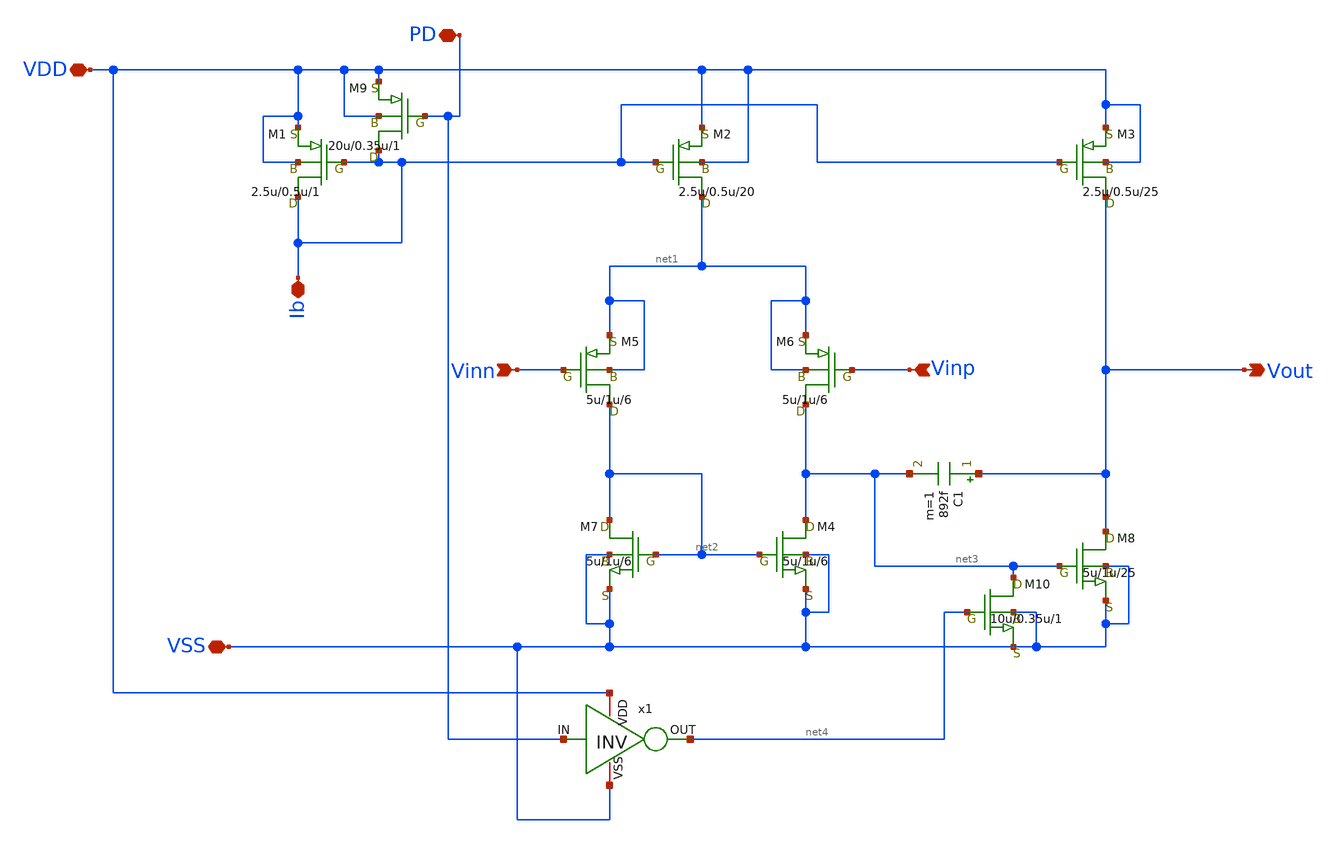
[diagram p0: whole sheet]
** sch_path: OPAmpP.sch
**.subckt OPAmpP Vout Vinn Vinp Ib VDD VSS PD
*.opin Vout
*.ipin Vinn
*.ipin Vinp
*.iopin Ib
*.iopin VDD
*.iopin VSS
*.iopin PD
M1 Ib Ib VDD VDD pch w=2.5u l=0.5u as=0 ps=0 ad=0 pd=0 m=1
M2 net1 Ib VDD VDD pch w=2.5u l=0.5u as=0 ps=0 ad=0 pd=0 m=20
M3 Vout Ib VDD VDD pch w=2.5u l=0.5u as=0 ps=0 ad=0 pd=0 m=25
M4 net3 net2 VSS VSS nch w=5u l=1u as=0 ps=0 ad=0 pd=0 m=6
M5 net2 Vinn net1 net1 pch w=5u l=1u as=0 ps=0 ad=0 pd=0 m=6
M6 net3 Vinp net1 net1 pch w=5u l=1u as=0 ps=0 ad=0 pd=0 m=6
M7 net2 net2 VSS VSS nch w=5u l=1u as=0 ps=0 ad=0 pd=0 m=6
M8 Vout net3 VSS VSS nch w=5u l=1u as=0 ps=0 ad=0 pd=0 m=25
C1 Vout net3 892f m=1
M9 Ib PD VDD VDD pch w=20u l=0.35u as=0 ps=0 ad=0 pd=0 m=1
M10 net3 net4 VSS VSS nch w=10u l=0.35u as=0 ps=0 ad=0 pd=0 m=1
x1 VDD net4 PD VSS INV
**.ends

* expanding   symbol:  INV.sym # of pins=4
** sym_path: INV.sym
** sch_path: INV.sch
.subckt INV VDD OUT IN VSS
*.opin OUT
*.ipin IN
*.iopin VDD
*.iopin VSS
M2 OUT IN VDD VDD pch w=10u l=0.35u as=0 ps=0 ad=0 pd=0 m=1
M1 OUT IN VSS VSS nch w=5u l=0.35u as=0 ps=0 ad=0 pd=0 m=1
.ends

.end
